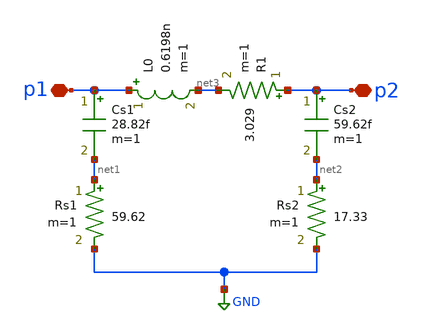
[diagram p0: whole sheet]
** sch_path: impedance-transformer/xschem/l1.sch
**.subckt l1 p2 p1
*.iopin p2
*.iopin p1
L0 p1 net3 0.6198n m=1
Cs1 p1 net1 28.82f m=1
Cs2 p2 net2 59.62f m=1
Rs1 net1 GND 59.62 m=1
Rs2 net2 GND 17.33 m=1
R1 p2 net3 3.029 m=1
**.ends
.GLOBAL GND
.end
